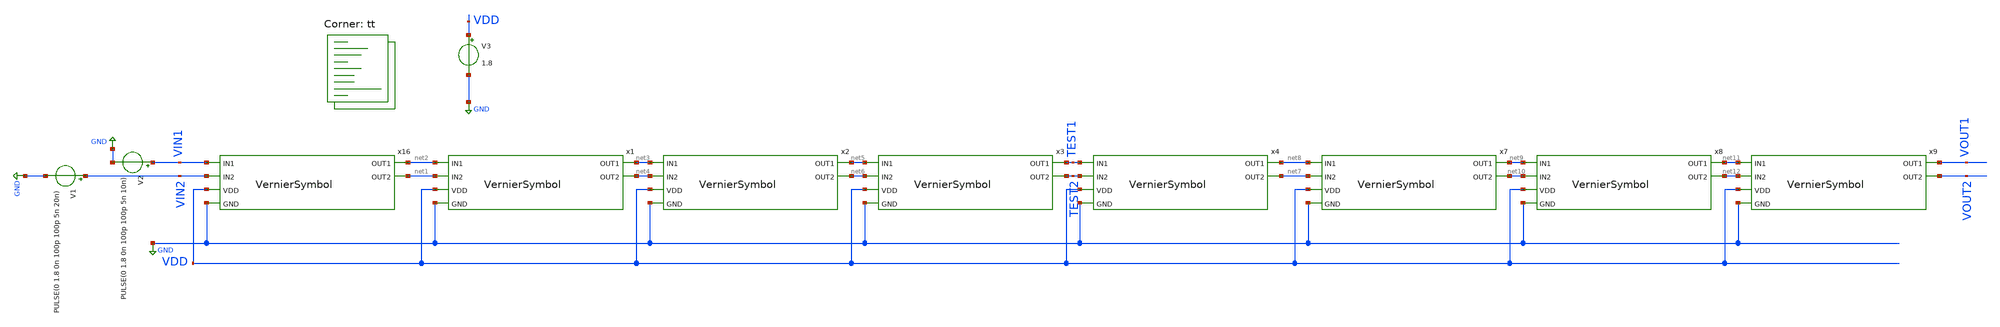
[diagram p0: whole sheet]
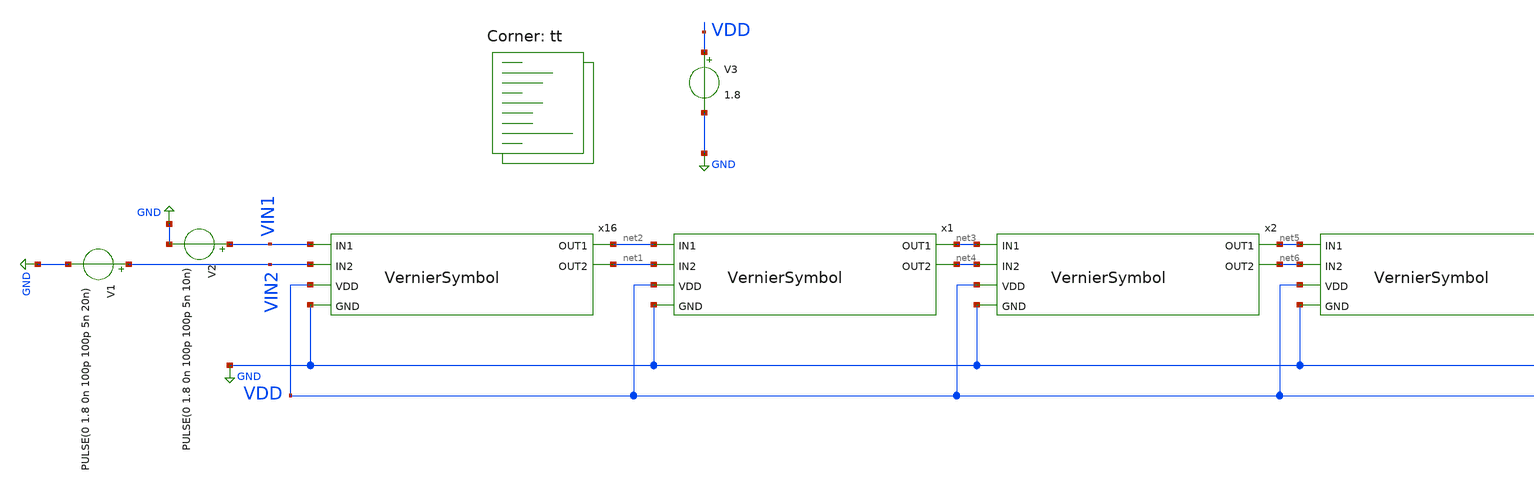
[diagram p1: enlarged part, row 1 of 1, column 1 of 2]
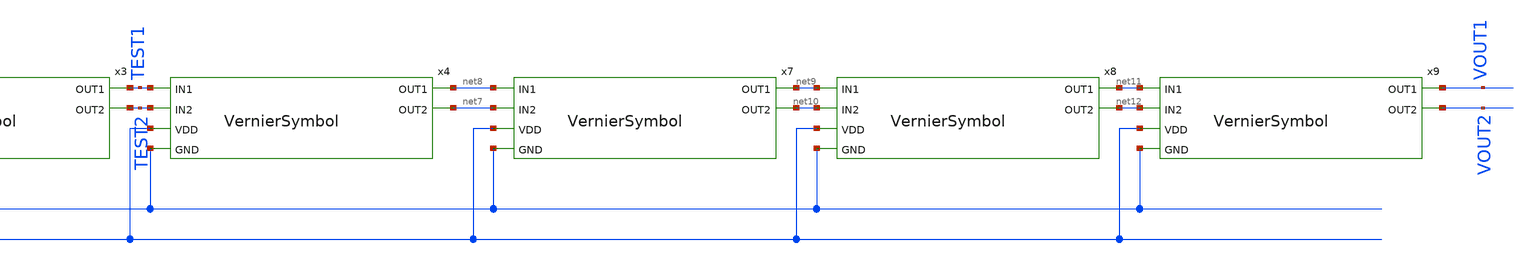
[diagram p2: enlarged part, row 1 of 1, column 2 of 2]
** sch_path: xschem/projects/VernierArray.sch
**.subckt VernierArray
V1 VIN2 GND PULSE(0 1.8 0n 100p 100p 5n 20n)
V2 VIN1 GND PULSE(0 1.8 0n 100p 100p 5n 10n)
V3 VDD GND 1.8
x16 net2 VIN1 net1 VIN2 VDD GND VernierSymbol
x1 net3 net2 net4 net1 VDD GND VernierSymbol
x2 net5 net3 net6 net4 VDD GND VernierSymbol
x3 TEST1 net5 TEST2 net6 VDD GND VernierSymbol
x4 net8 TEST1 net7 TEST2 VDD GND VernierSymbol
x7 net9 net8 net10 net7 VDD GND VernierSymbol
x8 net11 net9 net12 net10 VDD GND VernierSymbol
x9 VOUT1 net11 VOUT2 net12 VDD GND VernierSymbol
**** begin user architecture code


.include $PDK_ROOT/sky130B/libs.ref/sky130_fd_sc_hd/spice/sky130_fd_sc_hd.spice

.control
tran 10p 100n
write VernierDelay.raw
plot v(VOUT1) v(VOUT2) v(TEST1) V(TEST2)
.endc

.options acct list
.option numdgt=6


.lib $::SKYWATER_MODELS/sky130.lib.spice tt
**** end user architecture code
**.ends

* expanding   symbol:  VernierSymbol.sym # of pins=6
** sym_path: xschem/projects/VernierSymbol.sym
** sch_path: xschem/projects/VernierSymbol.sch
.subckt VernierSymbol OUT1 IN1 OUT2 IN2 VDD GND
*.ipin VDD
*.ipin GND
*.ipin IN1
*.ipin IN2
*.opin OUT1
*.opin OUT2
x2 net8 OUT2 0 0 VDD VDD OUT1 sky130_fd_sc_hd__dlxtp_1
x10 net5 GND GND VDD VDD net7 sky130_fd_sc_hd__buf_1
x11 net4 GND GND VDD VDD net5 sky130_fd_sc_hd__buf_1
x12 IN2 GND GND VDD VDD net4 sky130_fd_sc_hd__buf_1
x6 net3 GND GND VDD VDD net6 sky130_fd_sc_hd__buf_1
x7 net2 GND GND VDD VDD net3 sky130_fd_sc_hd__buf_1
x8 net1 GND GND VDD VDD net2 sky130_fd_sc_hd__buf_1
x9 IN1 GND GND VDD VDD net1 sky130_fd_sc_hd__buf_1
x5 net6 GND GND VDD VDD net8 sky130_fd_sc_hd__buf_1
x13 net7 GND GND VDD VDD OUT2 sky130_fd_sc_hd__buf_1
.ends

.GLOBAL GND
.end
